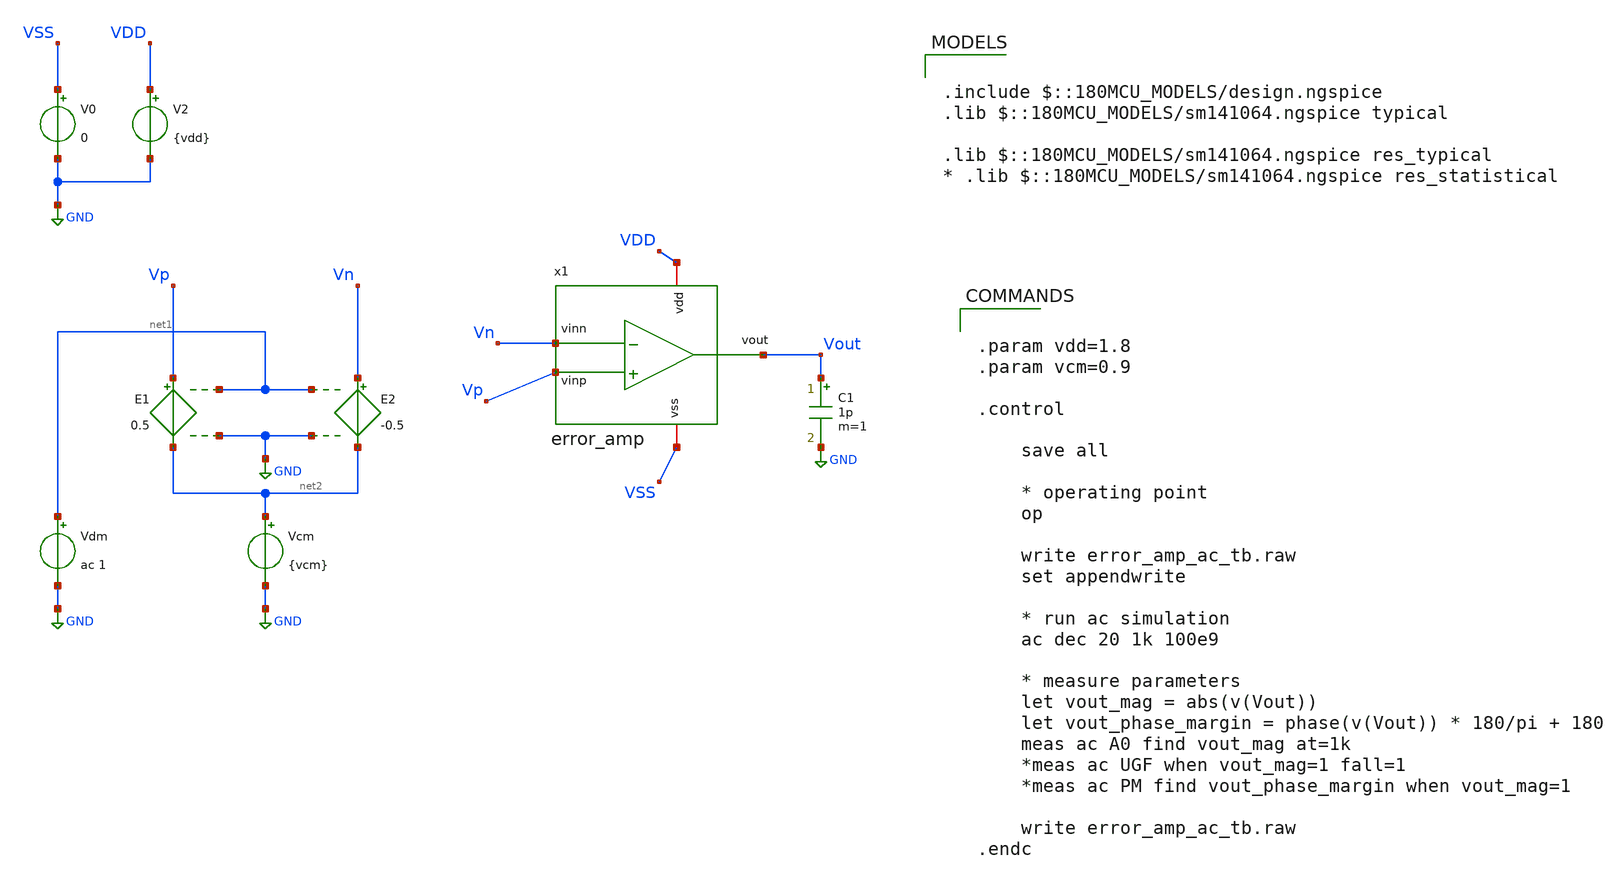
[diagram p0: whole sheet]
** sch_path: analog-db/drawings/ldo-005-ti-ldo-buffer-ref/gf180/error_amp/error_amp_ac_tb.sch
**.subckt error_amp_ac_tb
C1 Vout GND 1p m=1
V0 VSS GND 0
V2 VDD GND {vdd}
E1 Vp net2 net1 GND 0.5
E2 Vn net2 net1 GND -0.5
Vdm net1 GND ac 1
Vcm net2 GND {vcm}
x1 VDD Vout Vp Vn VSS error_amp
**** begin user architecture code


.param vdd=1.8
.param vcm=0.9

.control

    save all

    * operating point
    op

    write error_amp_ac_tb.raw
    set appendwrite

    * run ac simulation
    ac dec 20 1k 100e9

    * measure parameters
    let vout_mag = abs(v(Vout))
    let vout_phase_margin = phase(v(Vout)) * 180/pi + 180
    meas ac A0 find vout_mag at=1k
    *meas ac UGF when vout_mag=1 fall=1
    *meas ac PM find vout_phase_margin when vout_mag=1

    write error_amp_ac_tb.raw
.endc



.include $::180MCU_MODELS/design.ngspice
.lib $::180MCU_MODELS/sm141064.ngspice typical

.lib $::180MCU_MODELS/sm141064.ngspice res_typical
* .lib $::180MCU_MODELS/sm141064.ngspice res_statistical

**** end user architecture code
**.ends

* expanding   symbol:  ldo-005-ti-ldo-buffer-ref/gf180/error_amp/error_amp.sym # of pins=5
** sym_path: analog-db/circuits/amp_032_ti_ldo_error_selfbias/pdk/gf180mcu/schematic/error_amp.sym
** sch_path: analog-db/circuits/amp_032_ti_ldo_error_selfbias/pdk/gf180mcu/schematic/error_amp.sch
.subckt error_amp vdd vout vinp vinn vss
*.iopin vdd
*.iopin vss
*.ipin vinp
*.opin vout
*.ipin vinn
XM2 net_b vinp net_c vss nfet_06v0 L=0.7u W=68.542u nf=1 ad='int((nf+1)/2) * W/nf * 0.18u' as='int((nf+2)/2) * W/nf * 0.18u'
+ pd='2*int((nf+1)/2) * (W/nf + 0.18u)' ps='2*int((nf+2)/2) * (W/nf + 0.18u)' nrd='0.18u / W' nrs='0.18u / W'
+ sa=0 sb=0 sd=0 m=1
XM3m net_a net_d vdd vdd pfet_06v0 L=0.5u W=69.545u nf=1 ad='int((nf+1)/2) * W/nf * 0.18u' as='int((nf+2)/2) * W/nf * 0.18u'
+ pd='2*int((nf+1)/2) * (W/nf + 0.18u)' ps='2*int((nf+2)/2) * (W/nf + 0.18u)' nrd='0.18u / W' nrs='0.18u / W'
+ sa=0 sb=0 sd=0 m=1
XM4 net_f net_a net_d vdd pfet_06v0 L=0.5u W=10u nf=1 ad='int((nf+1)/2) * W/nf * 0.18u' as='int((nf+2)/2) * W/nf * 0.18u'
+ pd='2*int((nf+1)/2) * (W/nf + 0.18u)' ps='2*int((nf+2)/2) * (W/nf + 0.18u)' nrd='0.18u / W' nrs='0.18u / W'
+ sa=0 sb=0 sd=0 m=1
XM5 net_b net_d vdd vdd pfet_06v0 L=0.5u W=69.545u nf=1 ad='int((nf+1)/2) * W/nf * 0.18u' as='int((nf+2)/2) * W/nf * 0.18u'
+ pd='2*int((nf+1)/2) * (W/nf + 0.18u)' ps='2*int((nf+2)/2) * (W/nf + 0.18u)' nrd='0.18u / W' nrs='0.18u / W'
+ sa=0 sb=0 sd=0 m=1
XM6 vout net_b vdd vdd pfet_06v0 L=3.8349u W=20u nf=1 ad='int((nf+1)/2) * W/nf * 0.18u' as='int((nf+2)/2) * W/nf * 0.18u'
+ pd='2*int((nf+1)/2) * (W/nf + 0.18u)' ps='2*int((nf+2)/2) * (W/nf + 0.18u)' nrd='0.18u / W' nrs='0.18u / W'
+ sa=0 sb=0 sd=0 m=1
Cc net1 vout 6.7168p m=1
XRZ net_b net1 vdd ppolyf_u_3k r_width=1u r_length=9.476u m=1
XM1 net_a vinn net_c vss nfet_06v0 L=0.7u W=68.542u nf=1 ad='int((nf+1)/2) * W/nf * 0.18u' as='int((nf+2)/2) * W/nf * 0.18u'
+ pd='2*int((nf+1)/2) * (W/nf + 0.18u)' ps='2*int((nf+2)/2) * (W/nf + 0.18u)' nrd='0.18u / W' nrs='0.18u / W'
+ sa=0 sb=0 sd=0 m=1
XM_mirror_error_amp_ref net2 net2 vss vss nfet_06v0 L=2u W=34.533u nf=1 ad='int((nf+1)/2) * W/nf * 0.18u'
+ as='int((nf+2)/2) * W/nf * 0.18u' pd='2*int((nf+1)/2) * (W/nf + 0.18u)' ps='2*int((nf+2)/2) * (W/nf + 0.18u)'
+ nrd='0.18u / W' nrs='0.18u / W' sa=0 sb=0 sd=0 m=1
XM_mirror_f net_f net2 vss vss nfet_06v0 L=2u W=5u nf=1 ad='int((nf+1)/2) * W/nf * 0.18u' as='int((nf+2)/2) * W/nf * 0.18u'
+ pd='2*int((nf+1)/2) * (W/nf + 0.18u)' ps='2*int((nf+2)/2) * (W/nf + 0.18u)' nrd='0.18u / W' nrs='0.18u / W'
+ sa=0 sb=0 sd=0 m=1
XM_mirror_c net_c net2 vss vss nfet_06v0 L=2u W=34.533u nf=1 ad='int((nf+1)/2) * W/nf * 0.18u' as='int((nf+2)/2) * W/nf * 0.18u'
+ pd='2*int((nf+1)/2) * (W/nf + 0.18u)' ps='2*int((nf+2)/2) * (W/nf + 0.18u)' nrd='0.18u / W' nrs='0.18u / W'
+ sa=0 sb=0 sd=0 m=1
XM_mirror_ea_out vout net2 vss vss nfet_06v0 L=2u W=34.533u nf=1 ad='int((nf+1)/2) * W/nf * 0.18u' as='int((nf+2)/2) * W/nf * 0.18u'
+ pd='2*int((nf+1)/2) * (W/nf + 0.18u)' ps='2*int((nf+2)/2) * (W/nf + 0.18u)' nrd='0.18u / W' nrs='0.18u / W'
+ sa=0 sb=0 sd=0 m=1
XM_bias net2 net2 vdd vdd pfet_06v0 L=2u W=6.3111u nf=1 ad='int((nf+1)/2) * W/nf * 0.18u' as='int((nf+2)/2) * W/nf * 0.18u'
+ pd='2*int((nf+1)/2) * (W/nf + 0.18u)' ps='2*int((nf+2)/2) * (W/nf + 0.18u)' nrd='0.18u / W' nrs='0.18u / W'
+ sa=0 sb=0 sd=0 m=1
.ends

.GLOBAL GND
.end
